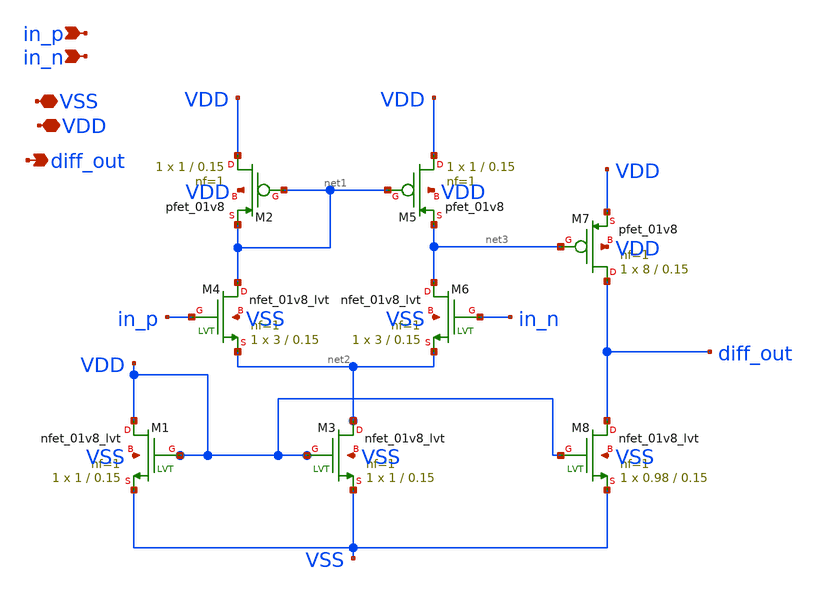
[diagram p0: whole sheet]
** sch_path: xschem/APD_amp.sch
**.subckt APD_amp VDD in_n in_p diff_out VSS
*.iopin VDD
*.ipin in_n
*.ipin in_p
*.opin diff_out
*.iopin VSS
XM3 net2 VDD VSS VSS sky130_fd_pr__nfet_01v8_lvt L=0.15 W=1 nf=1 ad='int((nf+1)/2) * W/nf * 0.29' as='int((nf+2)/2) * W/nf * 0.29'
+ pd='2*int((nf+1)/2) * (W/nf + 0.29)' ps='2*int((nf+2)/2) * (W/nf + 0.29)' nrd='0.29 / W' nrs='0.29 / W'
+ sa=0 sb=0 sd=0 mult=1 m=1
XM1 VDD VDD VSS VSS sky130_fd_pr__nfet_01v8_lvt L=0.15 W=1 nf=1 ad='int((nf+1)/2) * W/nf * 0.29' as='int((nf+2)/2) * W/nf * 0.29'
+ pd='2*int((nf+1)/2) * (W/nf + 0.29)' ps='2*int((nf+2)/2) * (W/nf + 0.29)' nrd='0.29 / W' nrs='0.29 / W'
+ sa=0 sb=0 sd=0 mult=1 m=1
XM2 VDD net1 net1 net4 sky130_fd_pr__pfet_01v8 L=0.15 W=1 nf=1 ad='int((nf+1)/2) * W/nf * 0.29' as='int((nf+2)/2) * W/nf * 0.29'
+ pd='2*int((nf+1)/2) * (W/nf + 0.29)' ps='2*int((nf+2)/2) * (W/nf + 0.29)' nrd='0.29 / W' nrs='0.29 / W'
+ sa=0 sb=0 sd=0 mult=1 m=1
XM5 VDD net1 net3 net5 sky130_fd_pr__pfet_01v8 L=0.15 W=1 nf=1 ad='int((nf+1)/2) * W/nf * 0.29' as='int((nf+2)/2) * W/nf * 0.29'
+ pd='2*int((nf+1)/2) * (W/nf + 0.29)' ps='2*int((nf+2)/2) * (W/nf + 0.29)' nrd='0.29 / W' nrs='0.29 / W'
+ sa=0 sb=0 sd=0 mult=1 m=1
XM6 net3 in_n net2 VSS sky130_fd_pr__nfet_01v8_lvt L=0.15 W=3 nf=1 ad='int((nf+1)/2) * W/nf * 0.29' as='int((nf+2)/2) * W/nf * 0.29'
+ pd='2*int((nf+1)/2) * (W/nf + 0.29)' ps='2*int((nf+2)/2) * (W/nf + 0.29)' nrd='0.29 / W' nrs='0.29 / W'
+ sa=0 sb=0 sd=0 mult=1 m=1
XM4 net1 in_p net2 VSS sky130_fd_pr__nfet_01v8_lvt L=0.15 W=3 nf=1 ad='int((nf+1)/2) * W/nf * 0.29' as='int((nf+2)/2) * W/nf * 0.29'
+ pd='2*int((nf+1)/2) * (W/nf + 0.29)' ps='2*int((nf+2)/2) * (W/nf + 0.29)' nrd='0.29 / W' nrs='0.29 / W'
+ sa=0 sb=0 sd=0 mult=1 m=1
XM7 diff_out net3 VDD VDD sky130_fd_pr__pfet_01v8 L=0.15 W=8 nf=1 ad='int((nf+1)/2) * W/nf * 0.29' as='int((nf+2)/2) * W/nf * 0.29'
+ pd='2*int((nf+1)/2) * (W/nf + 0.29)' ps='2*int((nf+2)/2) * (W/nf + 0.29)' nrd='0.29 / W' nrs='0.29 / W'
+ sa=0 sb=0 sd=0 mult=1 m=1
XM8 diff_out VDD VSS VSS sky130_fd_pr__nfet_01v8_lvt L=0.15 W=0.98 nf=1 ad='int((nf+1)/2) * W/nf * 0.29'
+ as='int((nf+2)/2) * W/nf * 0.29' pd='2*int((nf+1)/2) * (W/nf + 0.29)' ps='2*int((nf+2)/2) * (W/nf + 0.29)'
+ nrd='0.29 / W' nrs='0.29 / W' sa=0 sb=0 sd=0 mult=1 m=1
**.ends
.end
